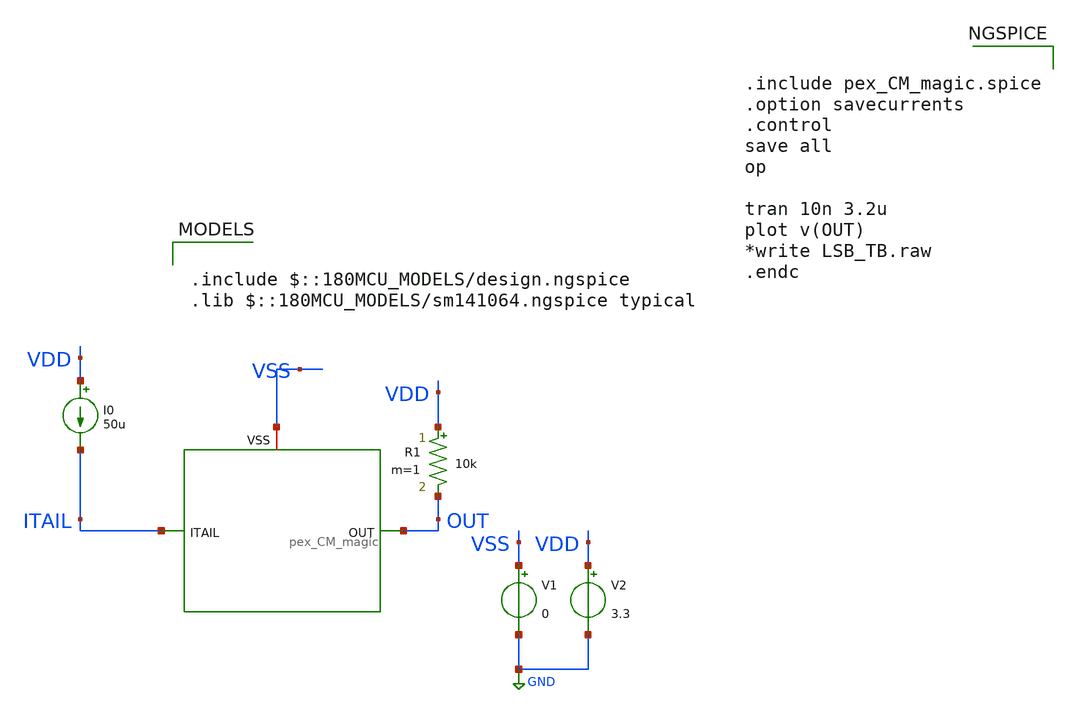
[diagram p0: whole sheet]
** sch_path: DAC_PAKISTAN_01/Pakistan1_Xschem/CM_tb.sch
**.subckt CM_tb
I0 VDD ITAIL 50u
V1 VSS GND 0
V2 VDD GND 3.3
R1 VDD OUT 10k m=1
x1 OUT ITAIL VSS pex_CM_magic
**** begin user architecture code

.include $::180MCU_MODELS/design.ngspice
.lib $::180MCU_MODELS/sm141064.ngspice typical



.include pex_CM_magic.spice
.option savecurrents
.control
save all
op

tran 10n 3.2u
plot v(OUT)
*write LSB_TB.raw
.endc


**** end user architecture code
**.ends
.GLOBAL GND
.end
